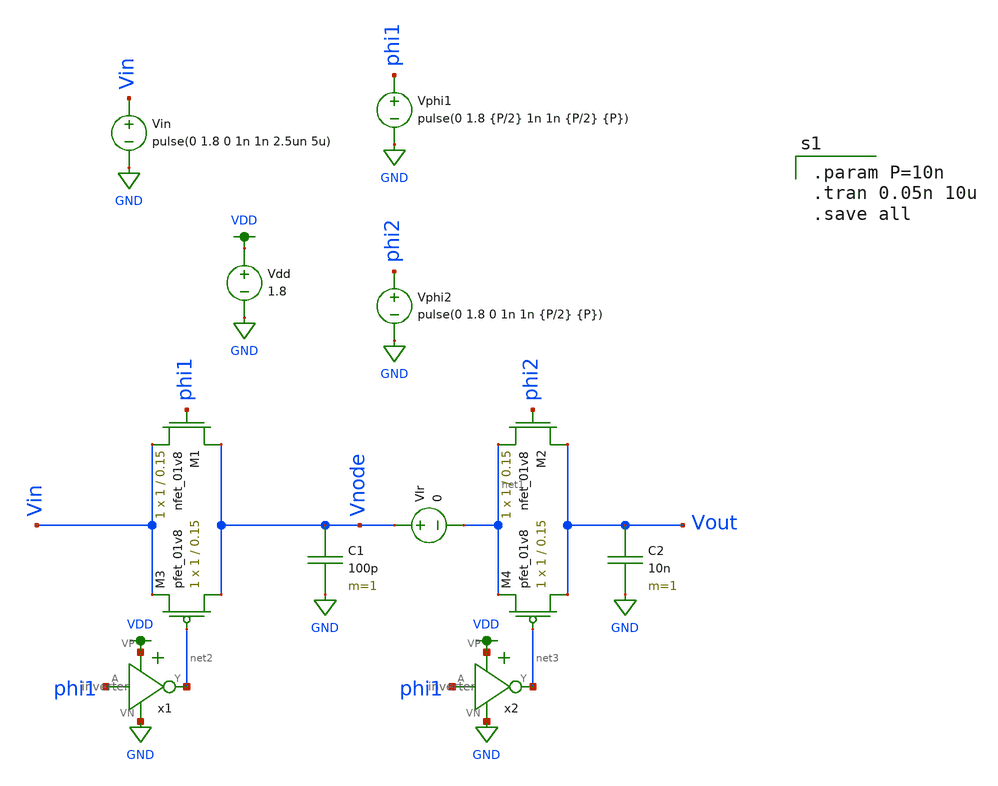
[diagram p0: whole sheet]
** sch_path: xschem/switched_capacitor/switched_capacitor_lpf.sch
**.subckt switched_capacitor_lpf
C1 Vnode GND 100p m=1
XM1 Vnode phi1 Vin GND sky130_fd_pr__nfet_01v8 L=0.15 W=1 nf=1 ad='int((nf+1)/2) * W/nf * 0.29' as='int((nf+2)/2) * W/nf * 0.29'
+ pd='2*int((nf+1)/2) * (W/nf + 0.29)' ps='2*int((nf+2)/2) * (W/nf + 0.29)' nrd='0.29 / W' nrs='0.29 / W'
+ sa=0 sb=0 sd=0 mult=1 m=1
XM2 Vout phi2 net1 GND sky130_fd_pr__nfet_01v8 L=0.15 W=1 nf=1 ad='int((nf+1)/2) * W/nf * 0.29' as='int((nf+2)/2) * W/nf * 0.29'
+ pd='2*int((nf+1)/2) * (W/nf + 0.29)' ps='2*int((nf+2)/2) * (W/nf + 0.29)' nrd='0.29 / W' nrs='0.29 / W'
+ sa=0 sb=0 sd=0 mult=1 m=1
Vphi1 phi1 GND pulse(0 1.8 {P/2} 1n 1n {P/2} {P})
Vphi2 phi2 GND pulse(0 1.8 0 1n 1n {P/2} {P})
Vdd VDD GND 1.8
VIr Vnode net1 0
C2 Vout GND 10n m=1
Vin Vin GND pulse(0 1.8 0 1n 1n 2.5un 5u)
XM3 Vnode net2 Vin VDD sky130_fd_pr__pfet_01v8 L=0.15 W=1 nf=1 ad='int((nf+1)/2) * W/nf * 0.29' as='int((nf+2)/2) * W/nf * 0.29'
+ pd='2*int((nf+1)/2) * (W/nf + 0.29)' ps='2*int((nf+2)/2) * (W/nf + 0.29)' nrd='0.29 / W' nrs='0.29 / W'
+ sa=0 sb=0 sd=0 mult=1 m=1
XM4 Vout net3 net1 VDD sky130_fd_pr__pfet_01v8 L=0.15 W=1 nf=1 ad='int((nf+1)/2) * W/nf * 0.29' as='int((nf+2)/2) * W/nf * 0.29'
+ pd='2*int((nf+1)/2) * (W/nf + 0.29)' ps='2*int((nf+2)/2) * (W/nf + 0.29)' nrd='0.29 / W' nrs='0.29 / W'
+ sa=0 sb=0 sd=0 mult=1 m=1
x1 VDD phi1 net2 GND inverter
x2 VDD phi1 net3 GND inverter
**** begin user architecture code

.option wnflag=1
.param MC_SWITCH=0.0
.lib ~/skywater/skywater-pdk/libraries/sky130_fd_pr_ngspice/latest/models/sky130.lib.spice tt


.param P=10n
.tran 0.05n 10u
.save all

**** end user architecture code
**.ends

* expanding   symbol:  /home/madvlsi/dev/git/magic-dds/xschem/other_project_files/inverter.sym # of
*+ pins=4
** sym_path: xschem/other_project_files/inverter.sym
** sch_path: xschem/other_project_files/inverter.sch
.subckt inverter VP A Y VN
*.iopin VP
*.iopin VN
*.ipin A
*.opin Y
XM1 Y A VN VN sky130_fd_pr__nfet_01v8 L=0.15 W=1 nf=1 ad='int((nf+1)/2) * W/nf * 0.29' as='int((nf+2)/2) * W/nf * 0.29'
+ pd='2*int((nf+1)/2) * (W/nf + 0.29)' ps='2*int((nf+2)/2) * (W/nf + 0.29)' nrd='0.29 / W' nrs='0.29 / W'
+ sa=0 sb=0 sd=0 mult=1 m=1
XM2 Y A VP VP sky130_fd_pr__pfet_01v8 L=0.15 W=4 nf=1 ad='int((nf+1)/2) * W/nf * 0.29' as='int((nf+2)/2) * W/nf * 0.29'
+ pd='2*int((nf+1)/2) * (W/nf + 0.29)' ps='2*int((nf+2)/2) * (W/nf + 0.29)' nrd='0.29 / W' nrs='0.29 / W'
+ sa=0 sb=0 sd=0 mult=1 m=1
.ends

.GLOBAL VDD
.GLOBAL GND
.end
